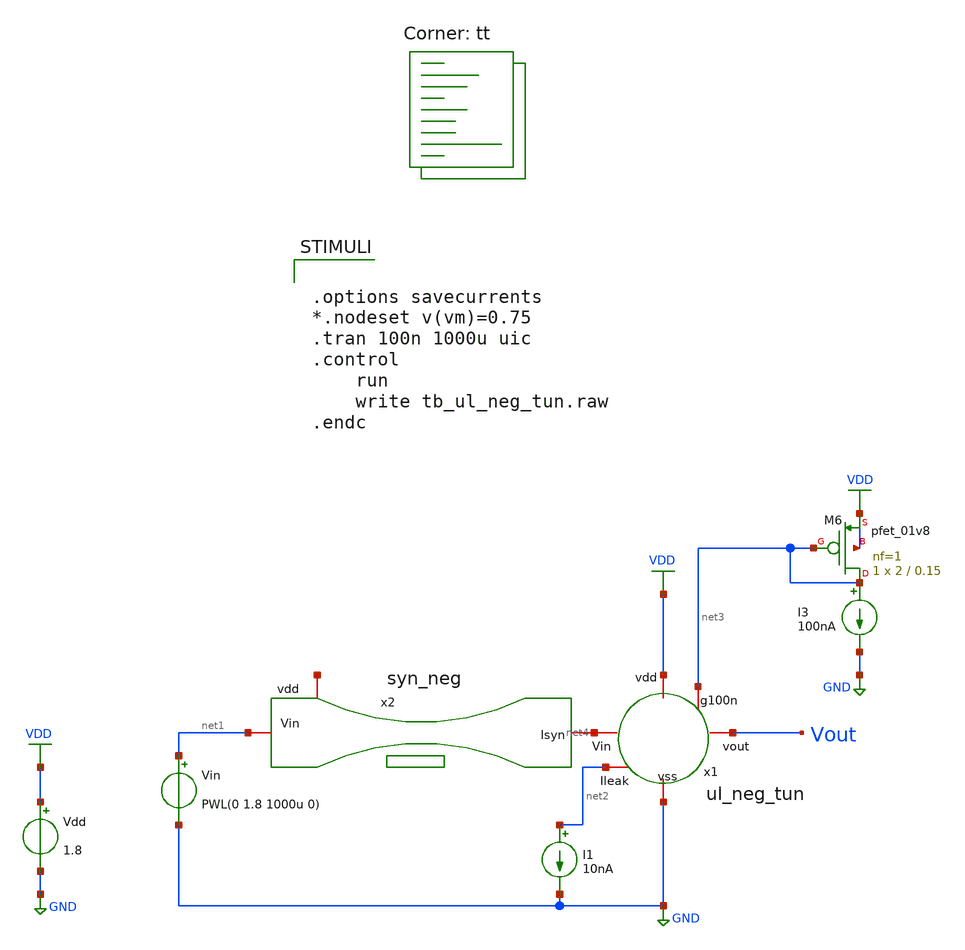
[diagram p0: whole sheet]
** sch_path: Neuron/ultralif/tb_ul_neg_tun.sch
**.subckt tb_ul_neg_tun
I1 net2 GND 10nA
Vdd VDD GND 1.8
I3 net3 GND 100nA
x1 net4 VDD net3 Vout net2 GND ul_neg_tun
Vin net1 GND PWL(0 1.8 1000u 0)
XM6 net3 net3 VDD VDD sky130_fd_pr__pfet_01v8 L=0.15 W=2 nf=1 ad='int((nf+1)/2) * W/nf * 0.29' as='int((nf+2)/2) * W/nf * 0.29'
+ pd='2*int((nf+1)/2) * (W/nf + 0.29)' ps='2*int((nf+2)/2) * (W/nf + 0.29)' nrd='0.29 / W' nrs='0.29 / W'
+ sa=0 sb=0 sd=0 mult=1 m=1
x2 net5 net1 net4 syn_neg
**** begin user architecture code
.lib $::SKYWATER_MODELS/sky130.lib.spice tt
**** end user architecture code
**.ends

* expanding   symbol:  ul_neg_tun.sym # of pins=6
** sym_path: Neuron/ultralif/ul_neg_tun.sym
** sch_path: Neuron/ultralif/ul_neg_tun.sch
.subckt ul_neg_tun Iext vdd g100n vout Ileak vss
*.iopin Iext
*.iopin vout
*.iopin vss
*.iopin Ileak
*.iopin vdd
*.iopin g100n
XM1 Ileak Ileak vm vdd sky130_fd_pr__pfet_01v8 L=10 W=1 nf=1 ad='int((nf+1)/2) * W/nf * 0.29' as='int((nf+2)/2) * W/nf * 0.29'
+ pd='2*int((nf+1)/2) * (W/nf + 0.29)' ps='2*int((nf+2)/2) * (W/nf + 0.29)' nrd='0.29 / W' nrs='0.29 / W'
+ sa=0 sb=0 sd=0 mult=1 m=1
XM2 Ileak net1 vm vdd sky130_fd_pr__pfet_01v8 L=0.15 W=1.5 nf=1 ad='int((nf+1)/2) * W/nf * 0.29' as='int((nf+2)/2) * W/nf * 0.29'
+ pd='2*int((nf+1)/2) * (W/nf + 0.29)' ps='2*int((nf+2)/2) * (W/nf + 0.29)' nrd='0.29 / W' nrs='0.29 / W'
+ sa=0 sb=0 sd=0 mult=1 m=1
XM3 net1 net1 vm vdd sky130_fd_pr__pfet_01v8 L=0.15 W=15 nf=1 ad='int((nf+1)/2) * W/nf * 0.29' as='int((nf+2)/2) * W/nf * 0.29'
+ pd='2*int((nf+1)/2) * (W/nf + 0.29)' ps='2*int((nf+2)/2) * (W/nf + 0.29)' nrd='0.29 / W' nrs='0.29 / W'
+ sa=0 sb=0 sd=0 mult=1 m=1
XM4 net1 Ileak vss vss sky130_fd_pr__nfet_01v8 L=4 W=1 nf=1 ad='int((1 + 1)/2) * 1 / 1 * 0.29' as='int((1 + 2)/2) * 1 / 1 * 0.29'
+ pd='2*int((1 + 1)/2) * (1 / 1 + 0.29)' ps='2*int((1 + 2)/2) * (1 / 1 + 0.29)' nrd='0.29 / 1 ' nrs='0.29 / 1 '
+ sa=0 sb=0 sd=0 mult=1 m=1
C1 vm vss 1p m=1
XM5 vout_n Ileak vss vss sky130_fd_pr__nfet_01v8 L=0.15 W=1 nf=1 ad='int((1 + 1)/2) * 1 / 1 * 0.29' as='int((1 + 2)/2) * 1 / 1 * 0.29'
+ pd='2*int((1 + 1)/2) * (1 / 1 + 0.29)' ps='2*int((1 + 2)/2) * (1 / 1 + 0.29)' nrd='0.29 / 1 ' nrs='0.29 / 1 '
+ sa=0 sb=0 sd=0 mult=1 m=1
XM6 vout_n g100n vdd vdd sky130_fd_pr__pfet_01v8 L=0.15 W=2 nf=1 ad='int((nf+1)/2) * W/nf * 0.29' as='int((nf+2)/2) * W/nf * 0.29'
+ pd='2*int((nf+1)/2) * (W/nf + 0.29)' ps='2*int((nf+2)/2) * (W/nf + 0.29)' nrd='0.29 / W' nrs='0.29 / W'
+ sa=0 sb=0 sd=0 mult=1 m=1
XM7 vout vout_n vss vss sky130_fd_pr__nfet_01v8 L=0.15 W=1 nf=1 ad='int((1 + 1)/2) * 1 / 1 * 0.29' as='int((1 + 2)/2) * 1 / 1 * 0.29'
+ pd='2*int((1 + 1)/2) * (1 / 1 + 0.29)' ps='2*int((1 + 2)/2) * (1 / 1 + 0.29)' nrd='0.29 / 1 ' nrs='0.29 / 1 '
+ sa=0 sb=0 sd=0 mult=1 m=1
XM8 vout vout_n vdd vdd sky130_fd_pr__pfet_01v8 L=0.15 W=2 nf=1 ad='int((nf+1)/2) * W/nf * 0.29' as='int((nf+2)/2) * W/nf * 0.29'
+ pd='2*int((nf+1)/2) * (W/nf + 0.29)' ps='2*int((nf+2)/2) * (W/nf + 0.29)' nrd='0.29 / W' nrs='0.29 / W'
+ sa=0 sb=0 sd=0 mult=1 m=1
XM9 vm Ileak Iext vdd sky130_fd_pr__pfet_01v8 L=0.15 W=2 nf=1 ad='int((nf+1)/2) * W/nf * 0.29' as='int((nf+2)/2) * W/nf * 0.29'
+ pd='2*int((nf+1)/2) * (W/nf + 0.29)' ps='2*int((nf+2)/2) * (W/nf + 0.29)' nrd='0.29 / W' nrs='0.29 / W'
+ sa=0 sb=0 sd=0 mult=1 m=1
.ends


* expanding   symbol:  syn_neg.sym # of pins=3
** sym_path: Neuron/ultralif/syn_neg.sym
** sch_path: Neuron/ultralif/syn_neg.sch
.subckt syn_neg vdd Vin Isyn
*.iopin Vin
*.iopin Isyn
*.iopin vdd
XM10 Isyn Vin vx vdd sky130_fd_pr__pfet_01v8 L=30 W=0.5 nf=1 ad='int((nf+1)/2) * W/nf * 0.29' as='int((nf+2)/2) * W/nf * 0.29'
+ pd='2*int((nf+1)/2) * (W/nf + 0.29)' ps='2*int((nf+2)/2) * (W/nf + 0.29)' nrd='0.29 / W' nrs='0.29 / W'
+ sa=0 sb=0 sd=0 mult=1 m=1
XM1 vx Vin vdd vdd sky130_fd_pr__pfet_01v8 L=30 W=0.5 nf=1 ad='int((nf+1)/2) * W/nf * 0.29' as='int((nf+2)/2) * W/nf * 0.29'
+ pd='2*int((nf+1)/2) * (W/nf + 0.29)' ps='2*int((nf+2)/2) * (W/nf + 0.29)' nrd='0.29 / W' nrs='0.29 / W'
+ sa=0 sb=0 sd=0 mult=1 m=1
.ends

.GLOBAL GND
.GLOBAL VDD
**** begin user architecture code


.options savecurrents
*.nodeset v(vm)=0.75
.tran 100n 1000u uic
.control
	run
	write tb_ul_neg_tun.raw
.endc


**** end user architecture code
.end
